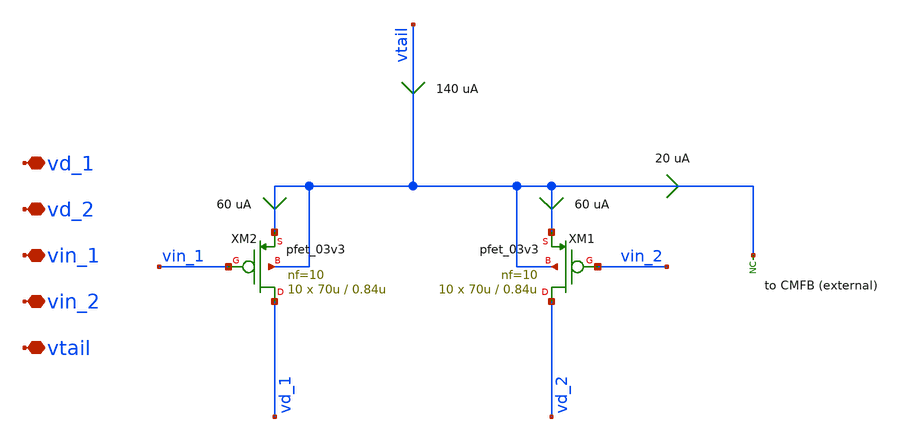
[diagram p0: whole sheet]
** sch_path: xschem/ccia_main_ota/b9_ccia_main_ota_s1_input_pair.sch
**.subckt b9_ccia_main_ota_s1_input_pair vd_1 vd_2 vin_1 vin_2 vtail
*.iopin vd_1
*.iopin vd_2
*.iopin vin_1
*.iopin vin_2
*.iopin vtail
XM2 vd_1 vin_1 vtail vtail pfet_03v3 L=0.84u W=70u nf=10 ad='int((nf+1)/2) * W/nf * 0.18u' as='int((nf+2)/2) * W/nf * 0.18u'
+ pd='2*int((nf+1)/2) * (W/nf + 0.18u)' ps='2*int((nf+2)/2) * (W/nf + 0.18u)' nrd='0.18u / W' nrs='0.18u / W'
+ sa=0 sb=0 sd=0 m=10
XM1 vd_2 vin_2 vtail vtail pfet_03v3 L=0.84u W=70u nf=10 ad='int((nf+1)/2) * W/nf * 0.18u' as='int((nf+2)/2) * W/nf * 0.18u'
+ pd='2*int((nf+1)/2) * (W/nf + 0.18u)' ps='2*int((nf+2)/2) * (W/nf + 0.18u)' nrd='0.18u / W' nrs='0.18u / W'
+ sa=0 sb=0 sd=0 m=10
* noconn vtail
**.ends
.end
